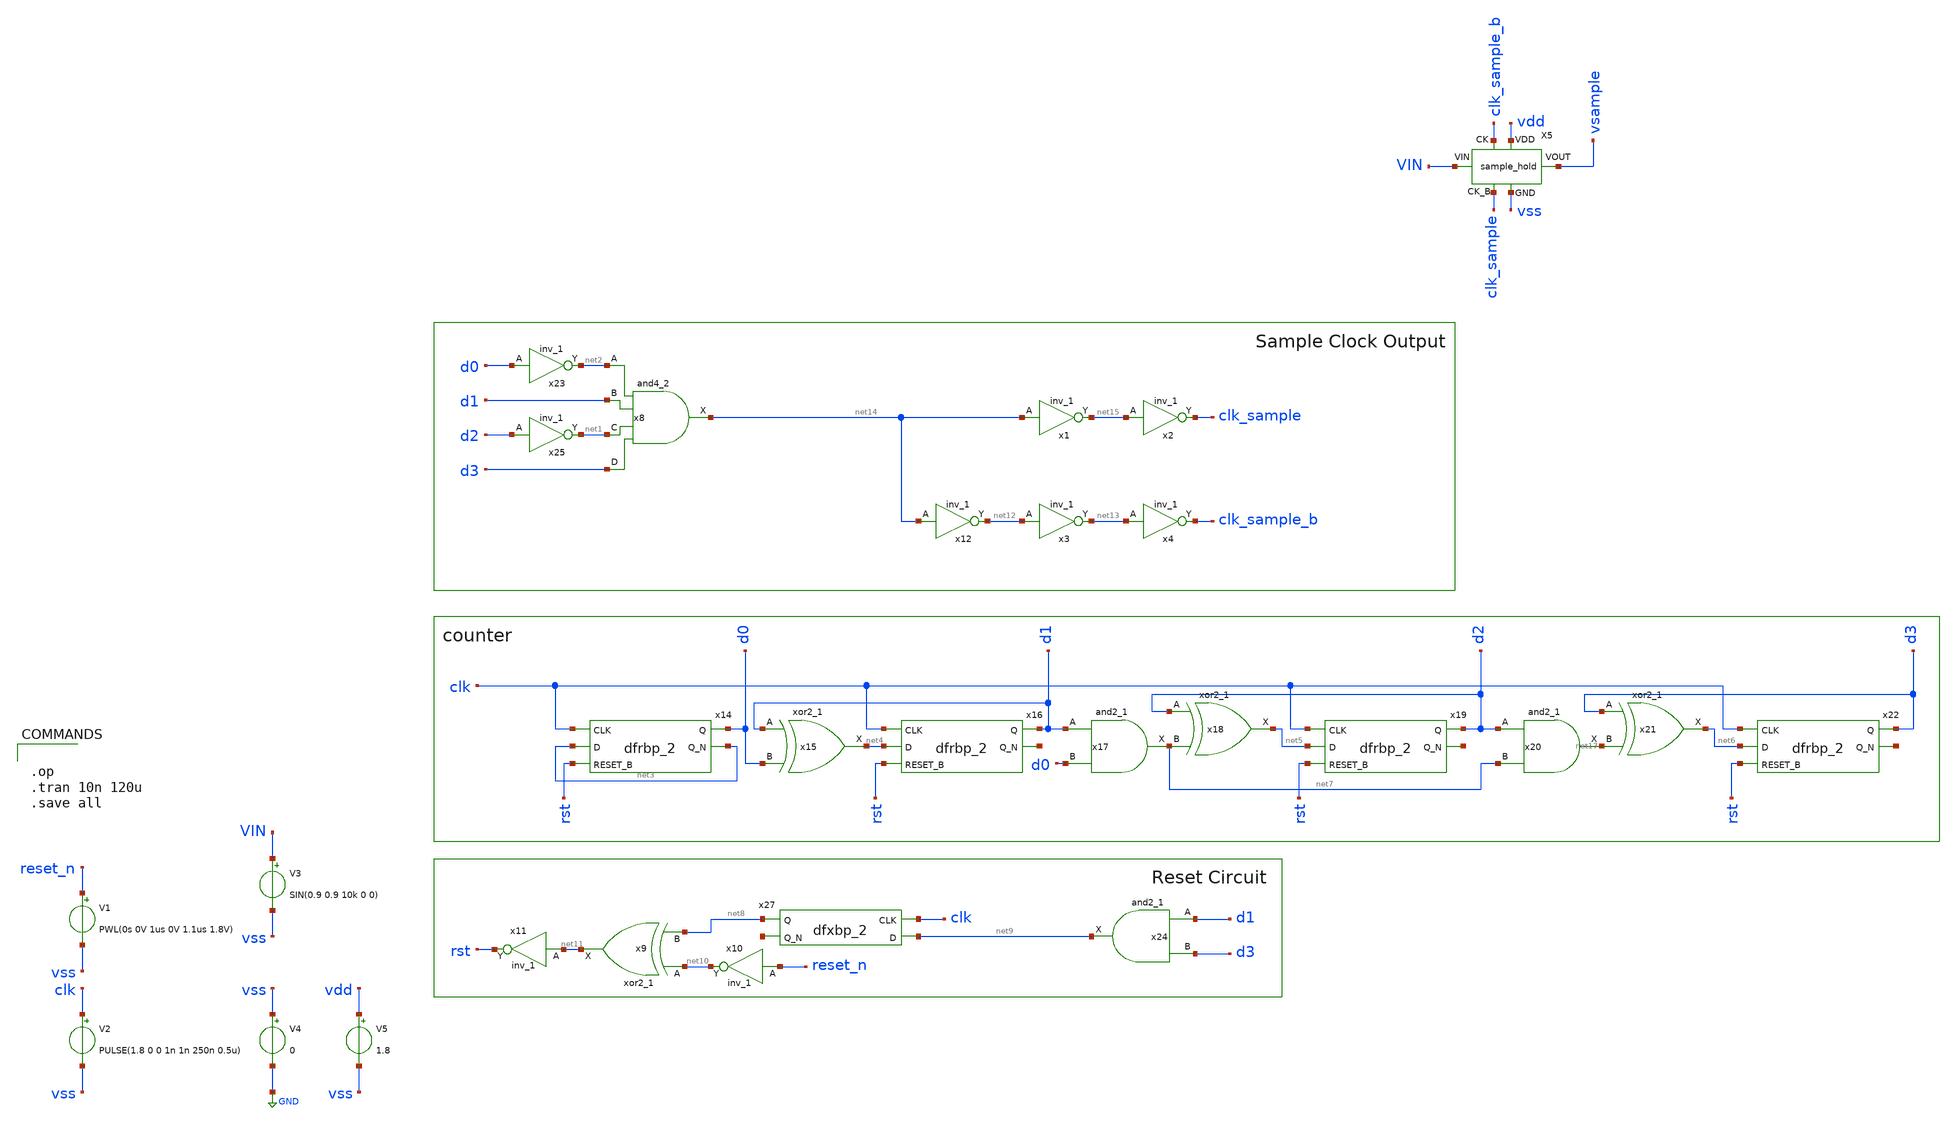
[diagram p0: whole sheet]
** sch_path: xschem/clockgen/clockgen_tb.sch
.lib $::SKYWATER_MODELS/sky130.lib.spice tt
.include $::SKYWATER_STDCELLS/sky130_fd_sc_hd.spice

**.subckt clockgen_tb
V2 clk vss PULSE(1.8 0 0 1n 1n 250n 0.5u)
V1 reset_n vss PWL(0s 0V 1us 0V 1.1us 1.8V)
V4 vss GND 0
V5 vdd vss 1.8
x8 net2 d1 net1 d3 vss vss vdd vdd net14 sky130_fd_sc_hd__and4_2
x14 clk net3 rst vss vss vdd vdd d0 net3 sky130_fd_sc_hd__dfrbp_2
x15 d1 d0 vss vss vdd vdd net4 sky130_fd_sc_hd__xor2_1
x16 clk net4 rst vss vss vdd vdd d1 net16 sky130_fd_sc_hd__dfrbp_2
x17 d1 d0 vss vss vdd vdd net7 sky130_fd_sc_hd__and2_1
x18 d2 net7 vss vss vdd vdd net5 sky130_fd_sc_hd__xor2_1
x20 d2 net7 vss vss vdd vdd net17 sky130_fd_sc_hd__and2_1
x21 d3 net17 vss vss vdd vdd net6 sky130_fd_sc_hd__xor2_1
x19 clk net5 rst vss vss vdd vdd d2 net18 sky130_fd_sc_hd__dfrbp_2
x22 clk net6 rst vss vss vdd vdd d3 net19 sky130_fd_sc_hd__dfrbp_2
x23 d0 vss vss vdd vdd net2 sky130_fd_sc_hd__inv_1
x25 d2 vss vss vdd vdd net1 sky130_fd_sc_hd__inv_1
x24 d1 d3 vss vss vdd vdd net9 sky130_fd_sc_hd__and2_1
x27 clk net9 vss vss vdd vdd net8 net20 sky130_fd_sc_hd__dfxbp_2
x9 net10 net8 vss vss vdd vdd net11 sky130_fd_sc_hd__xor2_1
x10 reset_n vss vss vdd vdd net10 sky130_fd_sc_hd__inv_1
x11 net11 vss vss vdd vdd rst sky130_fd_sc_hd__inv_1
x12 net14 vss vss vdd vdd net12 sky130_fd_sc_hd__inv_1
x1 net14 vss vss vdd vdd net15 sky130_fd_sc_hd__inv_1
x2 net15 vss vss vdd vdd clk_sample sky130_fd_sc_hd__inv_1
x3 net12 vss vss vdd vdd net13 sky130_fd_sc_hd__inv_1
x4 net13 vss vss vdd vdd clk_sample_b sky130_fd_sc_hd__inv_1
X5 vss vdd VIN vsample clk_sample_b clk_sample sample_hold
V3 VIN vss SIN(0.9 0.9 10k 0 0)
**** begin user architecture code


.op
.tran 10n 120u
.save all


**** end user architecture code
**.ends

* expanding   symbol:  xschem/sample/sample_hold.sym # of pins=6
** sym_path: xschem/sample/sample_hold.sym
** sch_path: xschem/sample/sample_hold.sch
.subckt sample_hold GND VDD VIN VOUT CK CK_B
*.iopin GND
*.iopin VDD
*.iopin CK
*.iopin CK_B
*.iopin VIN
*.iopin VOUT
XM4 net1 CK GND GND sky130_fd_pr__nfet_01v8 L=0.15 W=10 nf=1 ad='int((nf+1)/2) * W/nf * 0.29' as='int((nf+2)/2) * W/nf * 0.29'
+ pd='2*int((nf+1)/2) * (W/nf + 0.29)' ps='2*int((nf+2)/2) * (W/nf + 0.29)' nrd='0.29 / W' nrs='0.29 / W'
+ sa=0 sb=0 sd=0 mult=1 m=1
XM1 VOUT x VIN GND sky130_fd_pr__nfet_01v8 L=0.15 W=30 nf=1 ad='int((nf+1)/2) * W/nf * 0.29' as='int((nf+2)/2) * W/nf * 0.29'
+ pd='2*int((nf+1)/2) * (W/nf + 0.29)' ps='2*int((nf+2)/2) * (W/nf + 0.29)' nrd='0.29 / W' nrs='0.29 / W'
+ sa=0 sb=0 sd=0 mult=1 m=1
XM2 p x VDD p sky130_fd_pr__pfet_01v8 L=0.15 W=20 nf=1 ad='int((nf+1)/2) * W/nf * 0.29' as='int((nf+2)/2) * W/nf * 0.29'
+ pd='2*int((nf+1)/2) * (W/nf + 0.29)' ps='2*int((nf+2)/2) * (W/nf + 0.29)' nrd='0.29 / W' nrs='0.29 / W'
+ sa=0 sb=0 sd=0 mult=1 m=1
XM3 x net2 p p sky130_fd_pr__pfet_01v8 L=0.15 W=5 nf=1 ad='int((nf+1)/2) * W/nf * 0.29' as='int((nf+2)/2) * W/nf * 0.29'
+ pd='2*int((nf+1)/2) * (W/nf + 0.29)' ps='2*int((nf+2)/2) * (W/nf + 0.29)' nrd='0.29 / W' nrs='0.29 / W'
+ sa=0 sb=0 sd=0 mult=1 m=1
XM5 net2 CK_B VDD VDD sky130_fd_pr__pfet_01v8 L=0.15 W=2 nf=1 ad='int((nf+1)/2) * W/nf * 0.29' as='int((nf+2)/2) * W/nf * 0.29'
+ pd='2*int((nf+1)/2) * (W/nf + 0.29)' ps='2*int((nf+2)/2) * (W/nf + 0.29)' nrd='0.29 / W' nrs='0.29 / W'
+ sa=0 sb=0 sd=0 mult=1 m=1
XM6 net1 CK_B net2 GND sky130_fd_pr__nfet_01v8 L=0.15 W=1 nf=1 ad='int((nf+1)/2) * W/nf * 0.29' as='int((nf+2)/2) * W/nf * 0.29'
+ pd='2*int((nf+1)/2) * (W/nf + 0.29)' ps='2*int((nf+2)/2) * (W/nf + 0.29)' nrd='0.29 / W' nrs='0.29 / W'
+ sa=0 sb=0 sd=0 mult=1 m=1
XM7 VIN x net1 GND sky130_fd_pr__nfet_01v8 L=0.15 W=10 nf=1 ad='int((nf+1)/2) * W/nf * 0.29' as='int((nf+2)/2) * W/nf * 0.29'
+ pd='2*int((nf+1)/2) * (W/nf + 0.29)' ps='2*int((nf+2)/2) * (W/nf + 0.29)' nrd='0.29 / W' nrs='0.29 / W'
+ sa=0 sb=0 sd=0 mult=1 m=1
XM8 net2 x net1 GND sky130_fd_pr__nfet_01v8 L=0.15 W=5 nf=1 ad='int((nf+1)/2) * W/nf * 0.29' as='int((nf+2)/2) * W/nf * 0.29'
+ pd='2*int((nf+1)/2) * (W/nf + 0.29)' ps='2*int((nf+2)/2) * (W/nf + 0.29)' nrd='0.29 / W' nrs='0.29 / W'
+ sa=0 sb=0 sd=0 mult=1 m=1
XM9 x VDD net3 GND sky130_fd_pr__nfet_01v8 L=0.15 W=20 nf=1 ad='int((nf+1)/2) * W/nf * 0.29' as='int((nf+2)/2) * W/nf * 0.29'
+ pd='2*int((nf+1)/2) * (W/nf + 0.29)' ps='2*int((nf+2)/2) * (W/nf + 0.29)' nrd='0.29 / W' nrs='0.29 / W'
+ sa=0 sb=0 sd=0 mult=1 m=1
XM10 net3 CK GND GND sky130_fd_pr__nfet_01v8 L=0.15 W=20 nf=1 ad='int((nf+1)/2) * W/nf * 0.29' as='int((nf+2)/2) * W/nf * 0.29'
+ pd='2*int((nf+1)/2) * (W/nf + 0.29)' ps='2*int((nf+2)/2) * (W/nf + 0.29)' nrd='0.29 / W' nrs='0.29 / W'
+ sa=0 sb=0 sd=0 mult=1 m=1
XC9 p net1 sky130_fd_pr__cap_mim_m3_1 W=15 L=15 MF=1 m=1
XC1 VOUT GND sky130_fd_pr__cap_mim_m3_1 W=50 L=50 MF=1 m=1
.ends

.GLOBAL GND
.end
